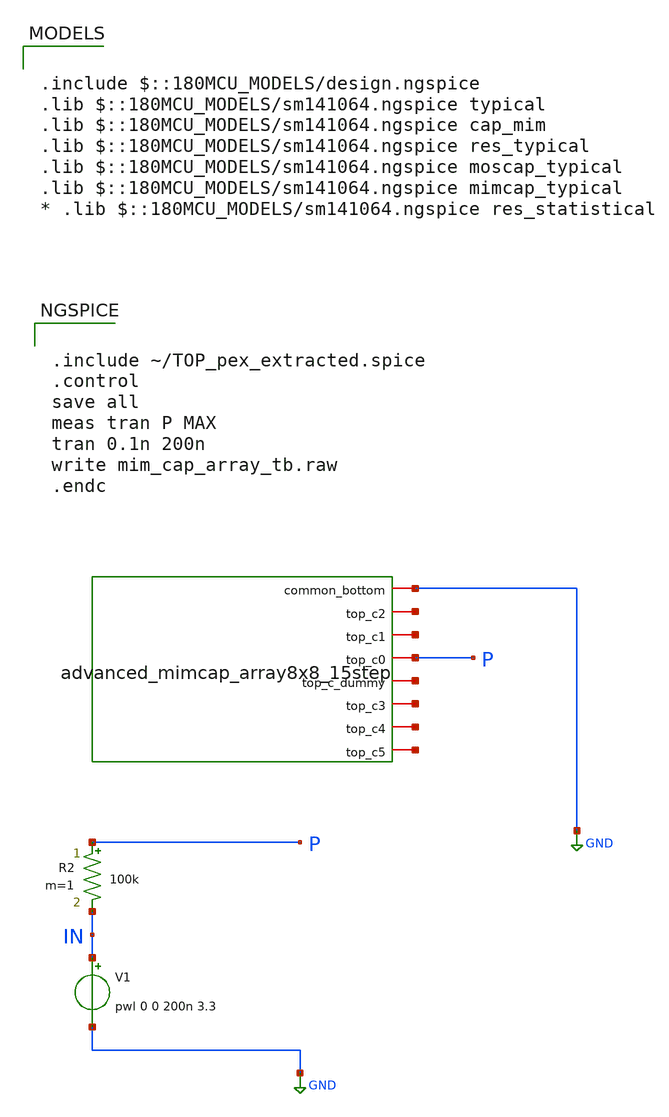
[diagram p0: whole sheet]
** sch_path: cdac/mim_cap_array_8x8/tb/mim_cap_array_tb.sch
* Copyright 2022 GlobalFoundries PDK Authors
* Licensed under the Apache License, Version 2.0 (the "License");
* you may not use this file except in compliance with the License.
* You may obtain a copy of the License at
* https://www.apache.org/licenses/LICENSE-2.0
* Unless required by applicable law or agreed to in writing, software
* distributed under the License is distributed on an "AS IS" BASIS,
* WITHOUT WARRANTIES OR CONDITIONS OF ANY KIND, either express or implied.
* See the License for the specific language governing permissions and
* limitations under the License.
**.subckt mim_cap_array_tb
V1 IN GND pwl 0 0 200n 3.3
R2 P IN 100k m=1
x1 net5 net4 net1 net3 P net2 GND TOP
**** begin user architecture code

.include $::180MCU_MODELS/design.ngspice
.lib $::180MCU_MODELS/sm141064.ngspice typical
.lib $::180MCU_MODELS/sm141064.ngspice cap_mim
.lib $::180MCU_MODELS/sm141064.ngspice res_typical
.lib $::180MCU_MODELS/sm141064.ngspice moscap_typical
.lib $::180MCU_MODELS/sm141064.ngspice mimcap_typical
* .lib $::180MCU_MODELS/sm141064.ngspice res_statistical



.include ~/TOP_pex_extracted.spice
.control
save all
meas tran P MAX
tran 0.1n 200n
write mim_cap_array_tb.raw
.endc


**** end user architecture code
**.ends
.GLOBAL GND
.end
